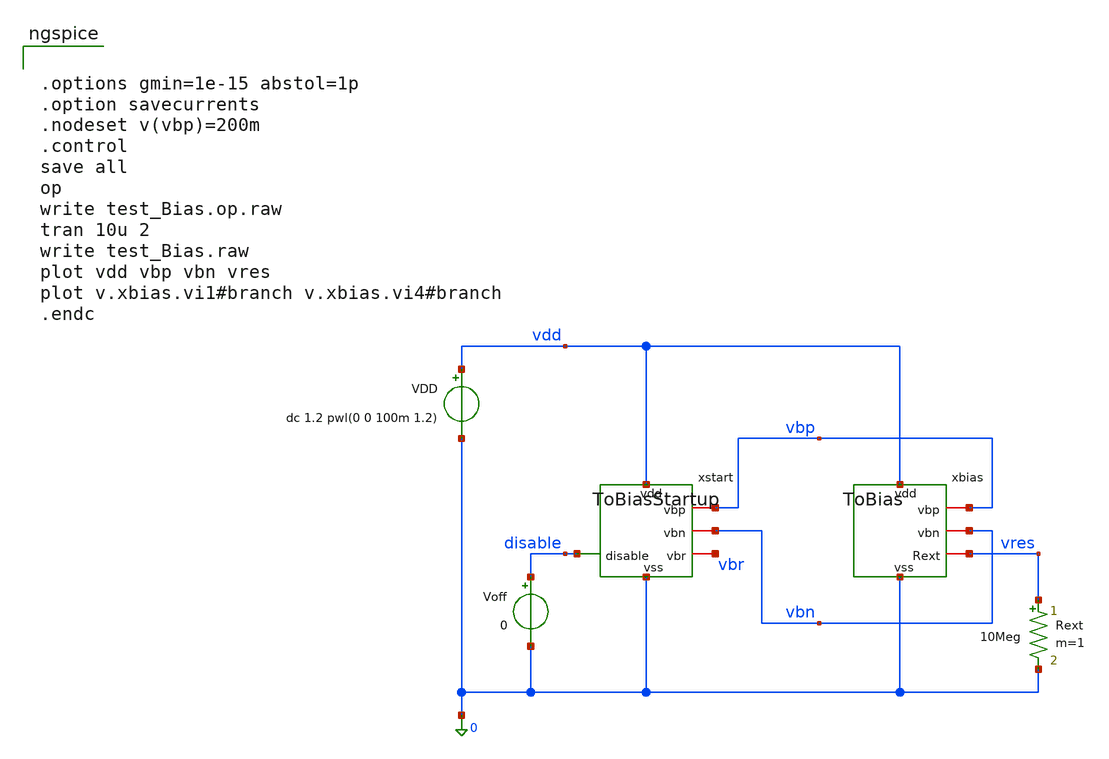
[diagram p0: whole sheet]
** sch_path: playground/test_Bias.sch
**.subckt test_Bias
xbias vdd vbp vbn vres 0 ToBias
xstart vdd vbp vbn disable vbr 0 ToBiasStartup
VDD vdd 0 dc 1.2 pwl(0 0 100m 1.2)
Voff disable 0 0
Rext vres 0 10Meg m=1
**** begin user architecture code


.options gmin=1e-15 abstol=1p
.option savecurrents
.nodeset v(vbp)=200m
.control
save all
op
write test_Bias.op.raw
tran 10u 2
write test_Bias.raw
plot vdd vbp vbn vres
plot v.xbias.vi1#branch v.xbias.vi4#branch
.endc


 .lib $::SKYWATER_MODELS/models/sky130.lib.spice tt

.param mc_mm_switch=0
.param mc_pr_switch=1


**** end user architecture code
**.ends

* expanding   symbol:  ToBias.sym # of pins=5
** sym_path: playground/ToBias.sym
** sch_path: playground/ToBias.sch
.subckt ToBias vdd vbp vbn Rext vss
*.iopin vss
*.iopin vdd
*.iopin vbp
*.iopin vbn
*.iopin Rext
XM10 net2 vbn Rext vss sky130_fd_pr__nfet_01v8 L=10 W=1 nf=1 ad='int((1 + 1)/2) * 1 / 1 * 0.29' as='int((1 + 2)/2) * 1 / 1 * 0.29'
+ pd='2*int((1 + 1)/2) * (1 / 1 + 0.29)' ps='2*int((1 + 2)/2) * (1 / 1 + 0.29)' nrd='0.29 / 1 ' nrs='0.29 / 1 '
+ sa=0 sb=0 sd=0 mult=4 m=4
XM12 vbp vbp vdd vdd sky130_fd_pr__pfet_01v8 L=10 W=1 nf=1 ad='int((nf+1)/2) * W/nf * 0.29' as='int((nf+2)/2) * W/nf * 0.29'
+ pd='2*int((nf+1)/2) * (W/nf + 0.29)' ps='2*int((nf+2)/2) * (W/nf + 0.29)' nrd='0.29 / W' nrs='0.29 / W'
+ sa=0 sb=0 sd=0 mult=1 m=1
XM11 vbn vbn vss vss sky130_fd_pr__nfet_01v8 L=10 W=1 nf=1 ad='int((1 + 1)/2) * 1 / 1 * 0.29' as='int((1 + 2)/2) * 1 / 1 * 0.29'
+ pd='2*int((1 + 1)/2) * (1 / 1 + 0.29)' ps='2*int((1 + 2)/2) * (1 / 1 + 0.29)' nrd='0.29 / 1 ' nrs='0.29 / 1 '
+ sa=0 sb=0 sd=0 mult=1 m=1
XM13 net1 vbp vdd vdd sky130_fd_pr__pfet_01v8 L=10 W=1 nf=1 ad='int((nf+1)/2) * W/nf * 0.29' as='int((nf+2)/2) * W/nf * 0.29'
+ pd='2*int((nf+1)/2) * (W/nf + 0.29)' ps='2*int((nf+2)/2) * (W/nf + 0.29)' nrd='0.29 / W' nrs='0.29 / W'
+ sa=0 sb=0 sd=0 mult=4 m=4
Vi1 vbp net2 0
.save i(vi1)
Vi4 net1 vbn 0
.save i(vi4)
.ends


* expanding   symbol:  ToBiasStartup.sym # of pins=6
** sym_path: ToBiasStartup.sym
** sch_path: ToBiasStartup.sch
.subckt ToBiasStartup vdd vbp vbn disable vbr vss
*.iopin vss
*.iopin vdd
*.iopin vbp
*.iopin vbn
*.iopin vbr
*.ipin disable
XM24 vbr disable vss vss sky130_fd_pr__nfet_01v8 L=0.3 W=1 nf=1 ad='int((1 + 1)/2) * 1 / 1 * 0.29' as='int((1 + 2)/2) * 1 / 1 * 0.29'
+ pd='2*int((1 + 1)/2) * (1 / 1 + 0.29)' ps='2*int((1 + 2)/2) * (1 / 1 + 0.29)' nrd='0.29 / 1 ' nrs='0.29 / 1 '
+ sa=0 sb=0 sd=0 mult=1 m=1
XM22 vbr vkick vdd vdd sky130_fd_pr__pfet_01v8 L=0.3 W=1 nf=1 ad='int((nf+1)/2) * W/nf * 0.29' as='int((nf+2)/2) * W/nf * 0.29'
+ pd='2*int((nf+1)/2) * (W/nf + 0.29)' ps='2*int((nf+2)/2) * (W/nf + 0.29)' nrd='0.29 / W' nrs='0.29 / W'
+ sa=0 sb=0 sd=0 mult=1 m=1
XM25 vkick vbp vdd vdd sky130_fd_pr__pfet_01v8 L=0.3 W=1 nf=1 ad='int((nf+1)/2) * W/nf * 0.29' as='int((nf+2)/2) * W/nf * 0.29'
+ pd='2*int((nf+1)/2) * (W/nf + 0.29)' ps='2*int((nf+2)/2) * (W/nf + 0.29)' nrd='0.29 / W' nrs='0.29 / W'
+ sa=0 sb=0 sd=0 mult=1 m=1
XM23 vbn disable vss vss sky130_fd_pr__nfet_01v8 L=0.3 W=1 nf=1 ad='int((1 + 1)/2) * 1 / 1 * 0.29' as='int((1 + 2)/2) * 1 / 1 * 0.29'
+ pd='2*int((1 + 1)/2) * (1 / 1 + 0.29)' ps='2*int((1 + 2)/2) * (1 / 1 + 0.29)' nrd='0.29 / 1 ' nrs='0.29 / 1 '
+ sa=0 sb=0 sd=0 mult=1 m=1
XM21 vbn vkick vdd vdd sky130_fd_pr__pfet_01v8 L=0.3 W=1 nf=1 ad='int((nf+1)/2) * W/nf * 0.29' as='int((nf+2)/2) * W/nf * 0.29'
+ pd='2*int((nf+1)/2) * (W/nf + 0.29)' ps='2*int((nf+2)/2) * (W/nf + 0.29)' nrd='0.29 / W' nrs='0.29 / W'
+ sa=0 sb=0 sd=0 mult=1 m=1
XM20 disable vkick disable vss sky130_fd_pr__nfet_01v8 L=40 W=40 nf=1 ad='int((1 + 1)/2) * 40 / 1 * 0.29'
+ as='int((1 + 2)/2) * 40 / 1 * 0.29' pd='2*int((1 + 1)/2) * (40 / 1 + 0.29)' ps='2*int((1 + 2)/2) * (40 / 1 + 0.29)'
+ nrd='0.29 / 40 ' nrs='0.29 / 40 ' sa=0 sb=0 sd=0 mult=1 m=1
XM26 vdd vbp vdd vss sky130_fd_pr__nfet_01v8 L=40 W=40 nf=1 ad='int((1 + 1)/2) * 40 / 1 * 0.29' as='int((1 + 2)/2) * 40 / 1 * 0.29'
+ pd='2*int((1 + 1)/2) * (40 / 1 + 0.29)' ps='2*int((1 + 2)/2) * (40 / 1 + 0.29)' nrd='0.29 / 40 ' nrs='0.29 / 40 '
+ sa=0 sb=0 sd=0 mult=1 m=1
.ends

.end
